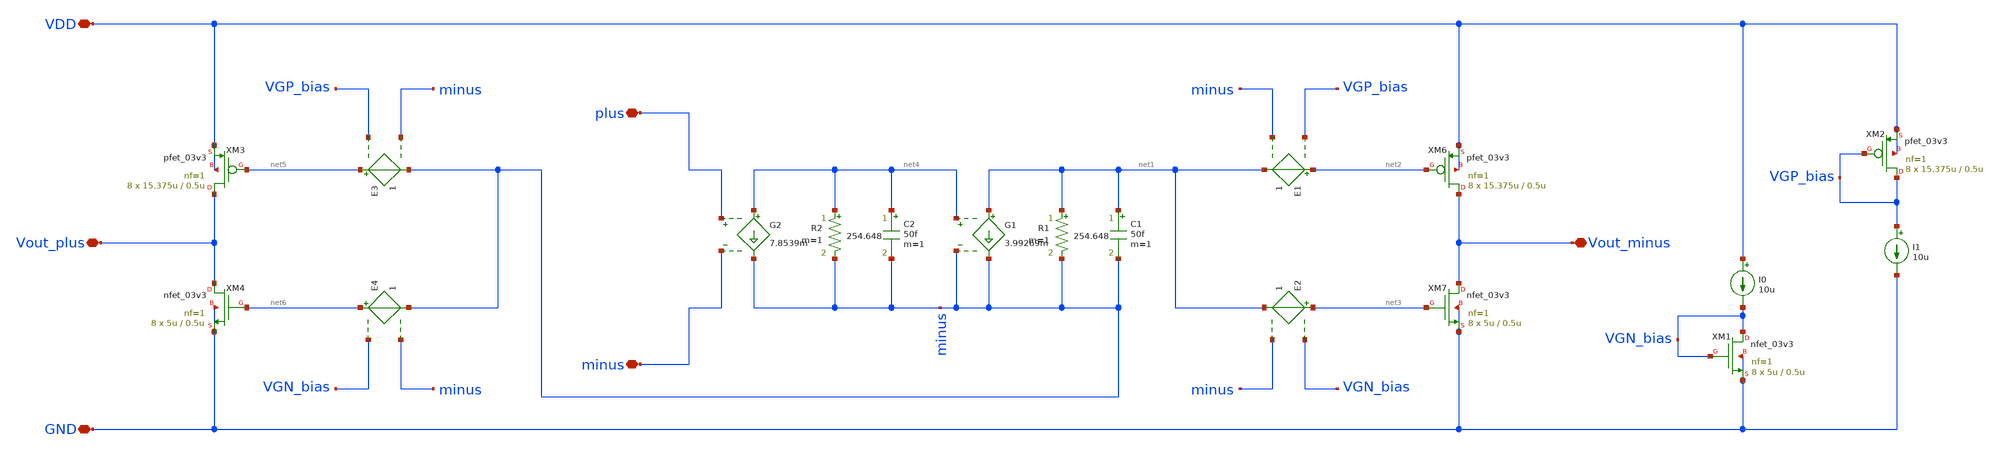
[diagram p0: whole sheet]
** sch_path: Design_Files/RAMP_Ideal/RAMP_Ideal_tb.sch
**.subckt RAMP_Ideal_tb plus minus Vout_minus Vout_plus VDD GND
*.iopin plus
*.iopin minus
*.iopin Vout_minus
*.iopin Vout_plus
*.iopin VDD
*.iopin GND
XM6 Vout_minus net2 VDD VDD pfet_03v3 L=0.5u W=15.375u nf=1 ad='int((nf+1)/2) * W/nf * 0.18u' as='int((nf+2)/2) * W/nf * 0.18u'
+ pd='2*int((nf+1)/2) * (W/nf + 0.18u)' ps='2*int((nf+2)/2) * (W/nf + 0.18u)' nrd='0.18u / W' nrs='0.18u / W'
+ sa=0 sb=0 sd=0 m=8
XM7 Vout_minus net3 GND GND nfet_03v3 L=0.5u W=5u nf=1 ad='int((nf+1)/2) * W/nf * 0.18u' as='int((nf+2)/2) * W/nf * 0.18u'
+ pd='2*int((nf+1)/2) * (W/nf + 0.18u)' ps='2*int((nf+2)/2) * (W/nf + 0.18u)' nrd='0.18u / W' nrs='0.18u / W'
+ sa=0 sb=0 sd=0 m=8
E1 net2 net1 VGP_bias minus 1
E2 net3 net1 VGN_bias minus 1
G1 net1 minus net4 minus 3.99269m
R1 net1 minus 254.648 m=1
C1 net1 minus 50f m=1
R2 net4 minus 254.648 m=1
C2 net4 minus 50f m=1
G2 net4 minus plus minus 7.8539m
XM1 VGN_bias VGN_bias GND GND nfet_03v3 L=0.5u W=5u nf=1 ad='int((nf+1)/2) * W/nf * 0.18u' as='int((nf+2)/2) * W/nf * 0.18u'
+ pd='2*int((nf+1)/2) * (W/nf + 0.18u)' ps='2*int((nf+2)/2) * (W/nf + 0.18u)' nrd='0.18u / W' nrs='0.18u / W'
+ sa=0 sb=0 sd=0 m=8
I0 VDD VGN_bias 10u
XM2 VGP_bias VGP_bias VDD VDD pfet_03v3 L=0.5u W=15.375u nf=1 ad='int((nf+1)/2) * W/nf * 0.18u' as='int((nf+2)/2) * W/nf * 0.18u'
+ pd='2*int((nf+1)/2) * (W/nf + 0.18u)' ps='2*int((nf+2)/2) * (W/nf + 0.18u)' nrd='0.18u / W' nrs='0.18u / W'
+ sa=0 sb=0 sd=0 m=8
I1 VGP_bias GND 10u
XM3 Vout_plus net5 VDD VDD pfet_03v3 L=0.5u W=15.375u nf=1 ad='int((nf+1)/2) * W/nf * 0.18u' as='int((nf+2)/2) * W/nf * 0.18u'
+ pd='2*int((nf+1)/2) * (W/nf + 0.18u)' ps='2*int((nf+2)/2) * (W/nf + 0.18u)' nrd='0.18u / W' nrs='0.18u / W'
+ sa=0 sb=0 sd=0 m=8
XM4 Vout_plus net6 GND GND nfet_03v3 L=0.5u W=5u nf=1 ad='int((nf+1)/2) * W/nf * 0.18u' as='int((nf+2)/2) * W/nf * 0.18u'
+ pd='2*int((nf+1)/2) * (W/nf + 0.18u)' ps='2*int((nf+2)/2) * (W/nf + 0.18u)' nrd='0.18u / W' nrs='0.18u / W'
+ sa=0 sb=0 sd=0 m=8
E3 net5 minus VGP_bias minus 1
E4 net6 minus VGN_bias minus 1
**.ends
.end
